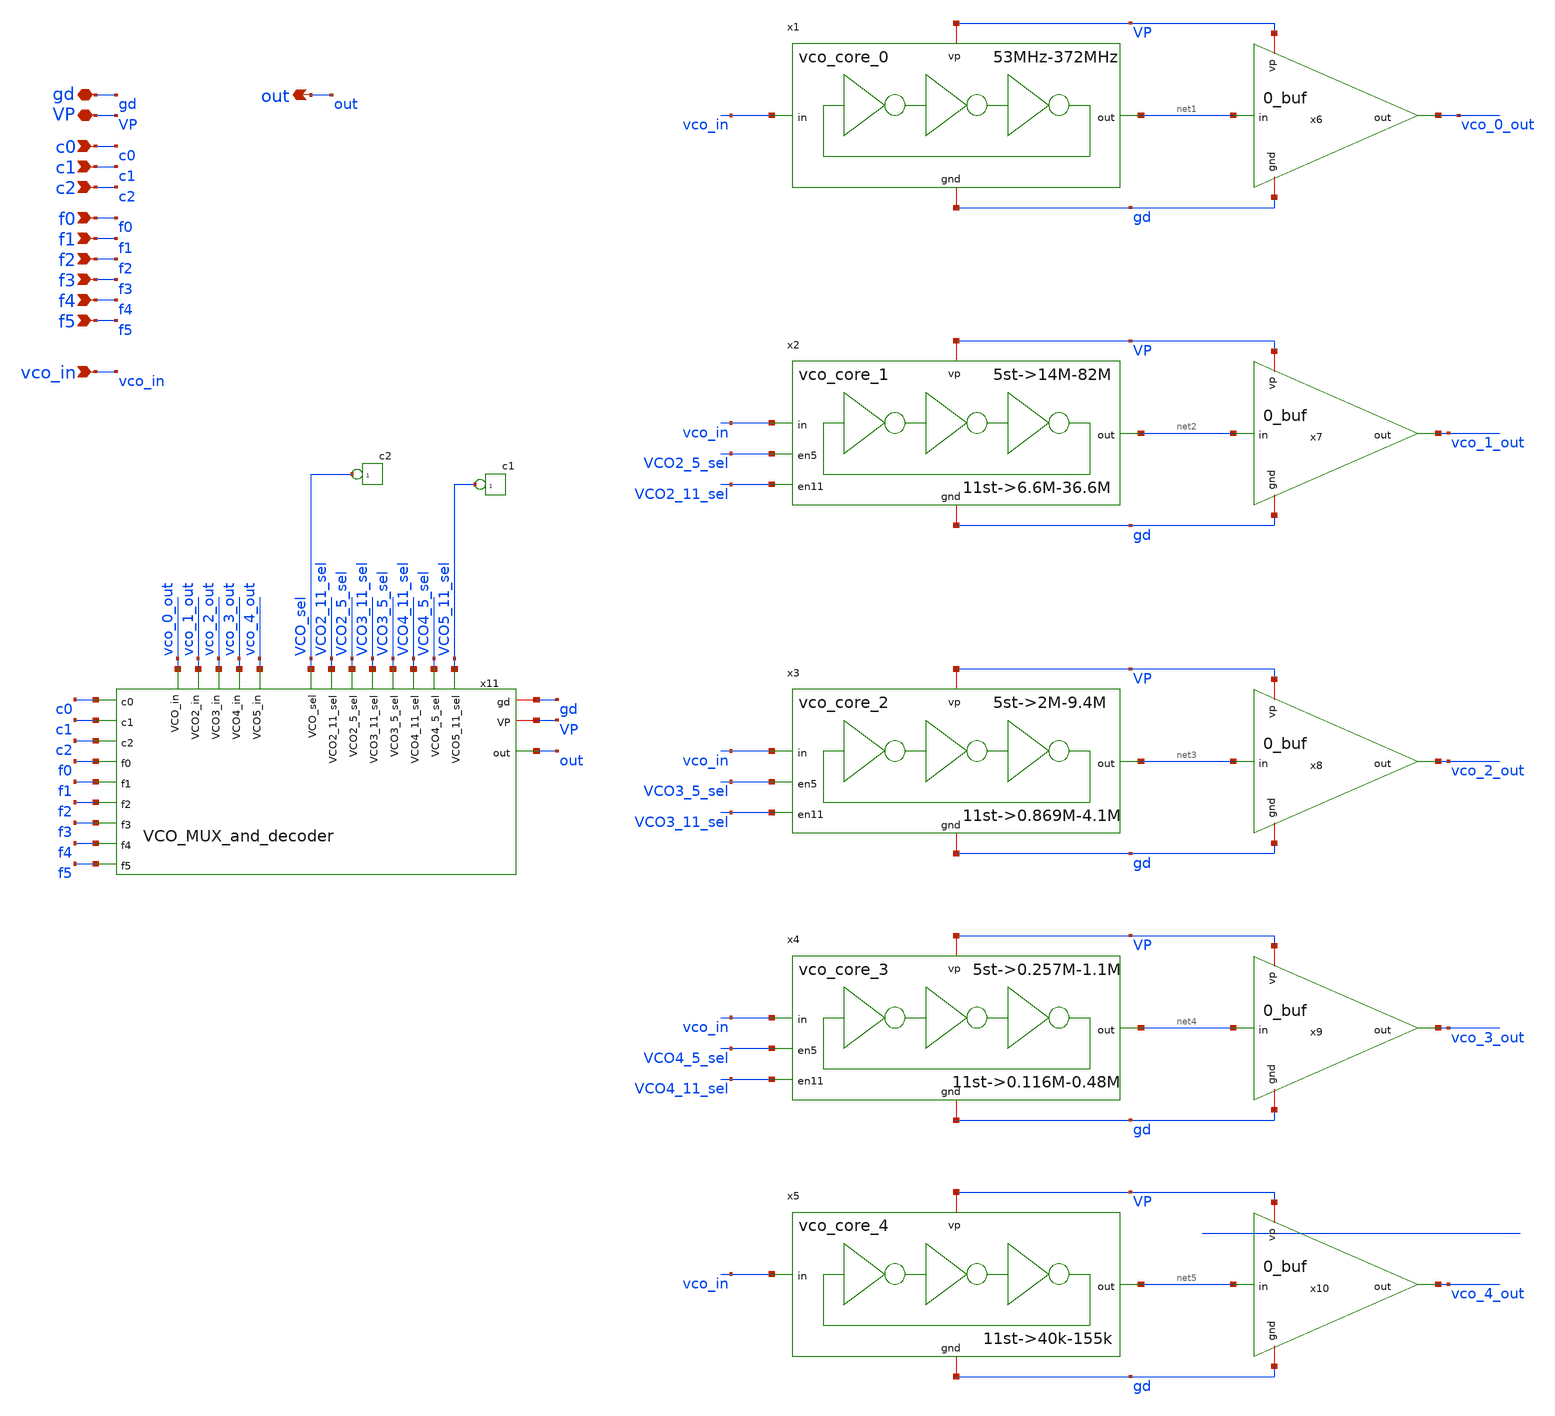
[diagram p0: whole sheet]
** sch_path: schematics/vco/vco_cell/vco_top.sch
**.subckt vco_top gd VP c1 c2 f0 f1 c0 f2 f3 f4 f5 out vco_in
*.iopin gd
*.iopin VP
*.ipin c1
*.ipin c2
*.ipin f0
*.ipin f1
*.ipin c0
*.ipin f2
*.ipin f3
*.ipin f4
*.ipin f5
*.opin out
*.ipin vco_in
x1 VP gd net1 vco_in vco_core_0
x2 VP gd net2 VCO2_5_sel vco_in VCO2_11_sel vco_core_1
x3 VP gd net3 VCO3_5_sel vco_in VCO3_11_sel vco_core_2
x4 VP gd net4 VCO4_5_sel vco_in VCO4_11_sel vco_core_3
x5 VP gd net5 vco_in vco_core_4
x6 VP gd vco_0_out net1 0_buf
x7 VP gd vco_1_out net2 0_buf
x8 VP gd vco_2_out net3 0_buf
x9 VP gd vco_3_out net4 0_buf
x10 VP gd vco_4_out net5 0_buf
x11 gd VP c0 c1 c2 f0 f1 f2 f3 f4 f5 vco_0_out vco_1_out vco_2_out vco_3_out vco_4_out VCO_sel
+ VCO2_11_sel VCO2_5_sel VCO3_11_sel VCO3_5_sel VCO4_11_sel VCO4_5_sel VCO5_11_sel out VCO_MUX_and_decoder
*connector(1,1) ?1 VCO_sel
*connector(1,1) ?1 VCO5_11_sel
**.ends
.end
